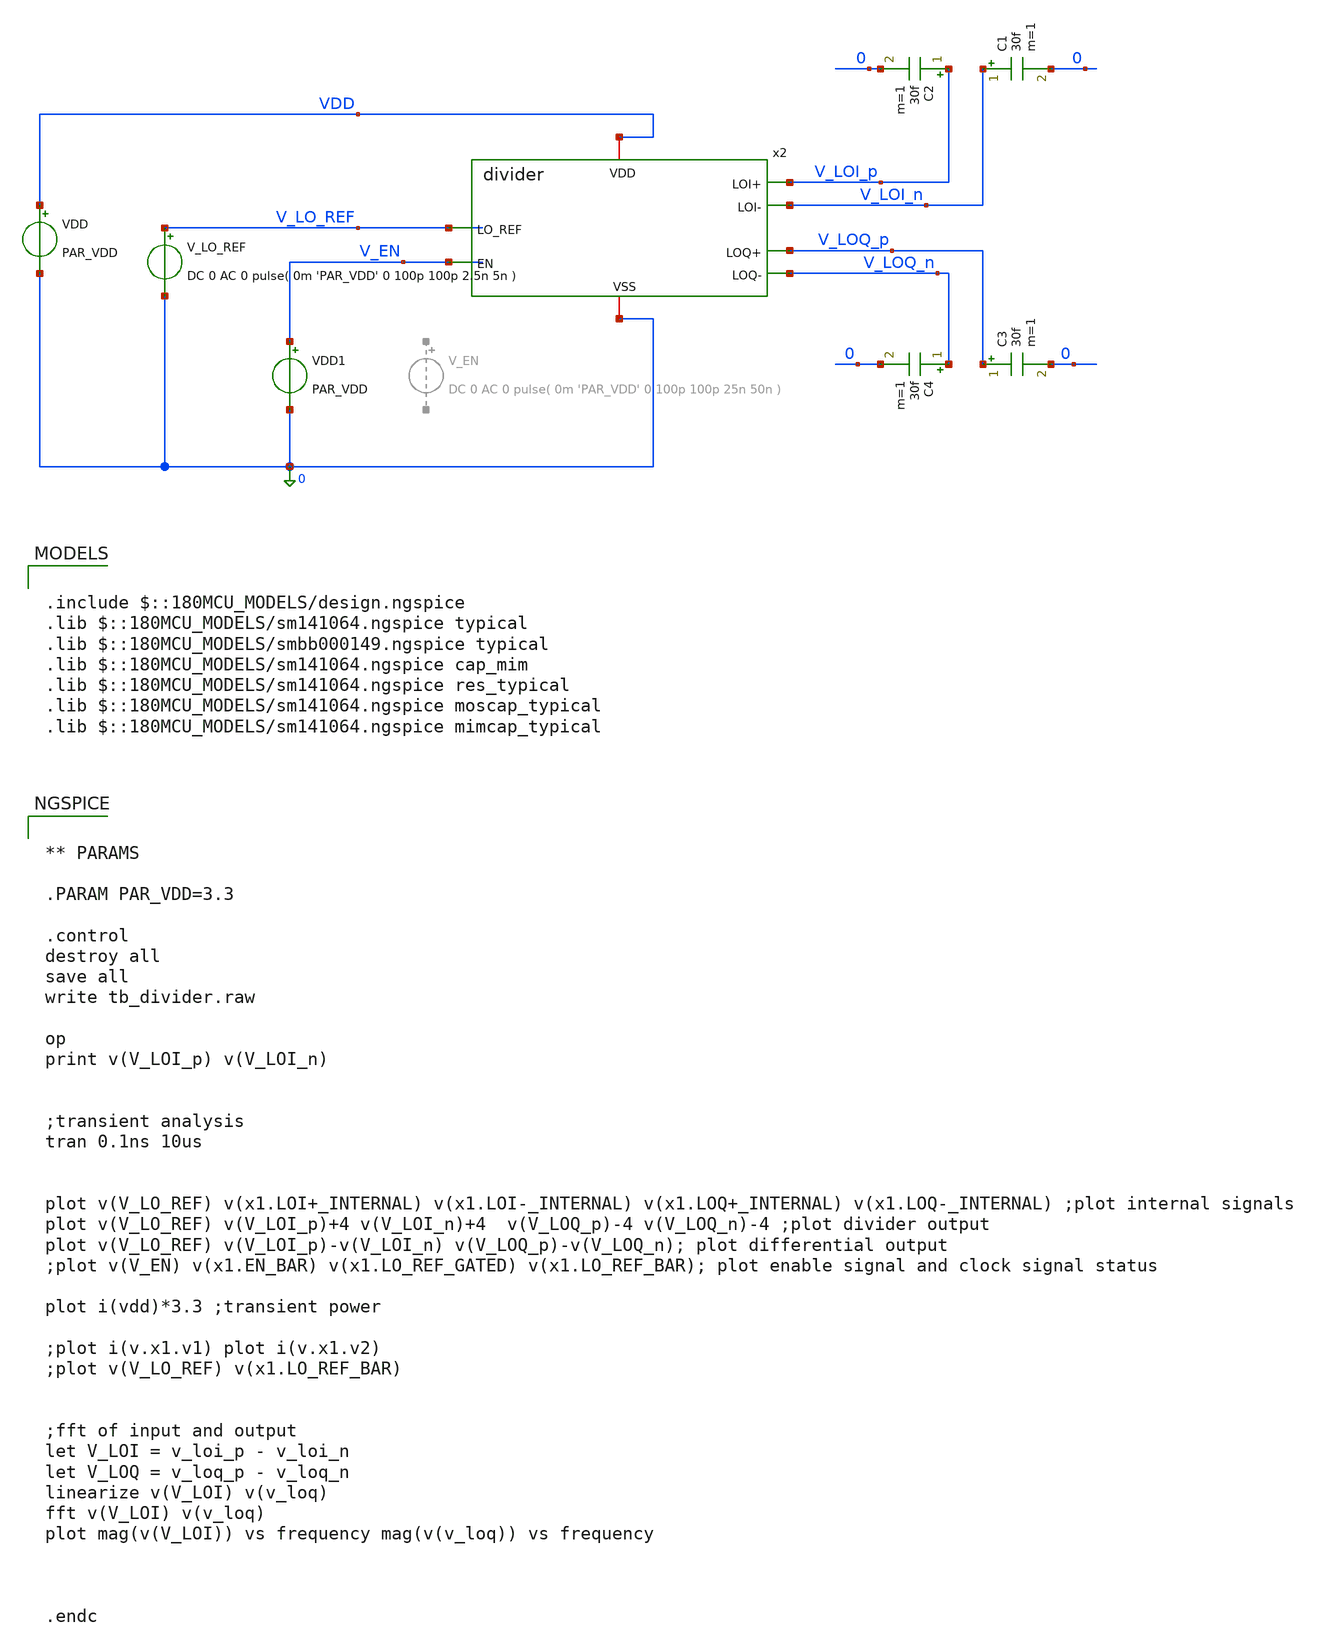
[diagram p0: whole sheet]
** sch_path: designs/divider/testbench/tb_divider.sch
**.subckt tb_divider
VDD VDD 0 PAR_VDD
V_LO_REF V_LO_REF 0 DC 0 AC 0 pulse( 0m 'PAR_VDD' 0 100p 100p 2.5n 5n )
C1 V_LOI_n 0 30f m=1
C2 V_LOI_p 0 30f m=1
C3 V_LOQ_p 0 30f m=1
C4 V_LOQ_n 0 30f m=1
VDD1 V_EN 0 PAR_VDD
x2 VDD 0 V_LO_REF V_LOI_p V_LOI_n V_LOQ_p V_LOQ_n V_EN divider
**** begin user architecture code

.include $::180MCU_MODELS/design.ngspice
.lib $::180MCU_MODELS/sm141064.ngspice typical
.lib $::180MCU_MODELS/smbb000149.ngspice typical
.lib $::180MCU_MODELS/sm141064.ngspice cap_mim
.lib $::180MCU_MODELS/sm141064.ngspice res_typical
.lib $::180MCU_MODELS/sm141064.ngspice moscap_typical
.lib $::180MCU_MODELS/sm141064.ngspice mimcap_typical



** PARAMS

.PARAM PAR_VDD=3.3

.control
destroy all
save all
write tb_divider.raw

op
print v(V_LOI_p) v(V_LOI_n)


;transient analysis
tran 0.1ns 10us


plot v(V_LO_REF) v(x1.LOI+_INTERNAL) v(x1.LOI-_INTERNAL) v(x1.LOQ+_INTERNAL) v(x1.LOQ-_INTERNAL)
+ ;plot internal signals
plot v(V_LO_REF) v(V_LOI_p)+4 v(V_LOI_n)+4  v(V_LOQ_p)-4 v(V_LOQ_n)-4 ;plot divider output
plot v(V_LO_REF) v(V_LOI_p)-v(V_LOI_n) v(V_LOQ_p)-v(V_LOQ_n); plot differential output
;plot v(V_EN) v(x1.EN_BAR) v(x1.LO_REF_GATED) v(x1.LO_REF_BAR); plot enable signal and clock signal
+ status

plot i(vdd)*3.3 ;transient power

;plot i(v.x1.v1) plot i(v.x1.v2)
;plot v(V_LO_REF) v(x1.LO_REF_BAR)


;fft of input and output
let V_LOI = v_loi_p - v_loi_n
let V_LOQ = v_loq_p - v_loq_n
linearize v(V_LOI) v(v_loq)
fft v(V_LOI) v(v_loq)
plot mag(v(V_LOI)) vs frequency mag(v(v_loq)) vs frequency



.endc


**** end user architecture code
**.ends
.end
